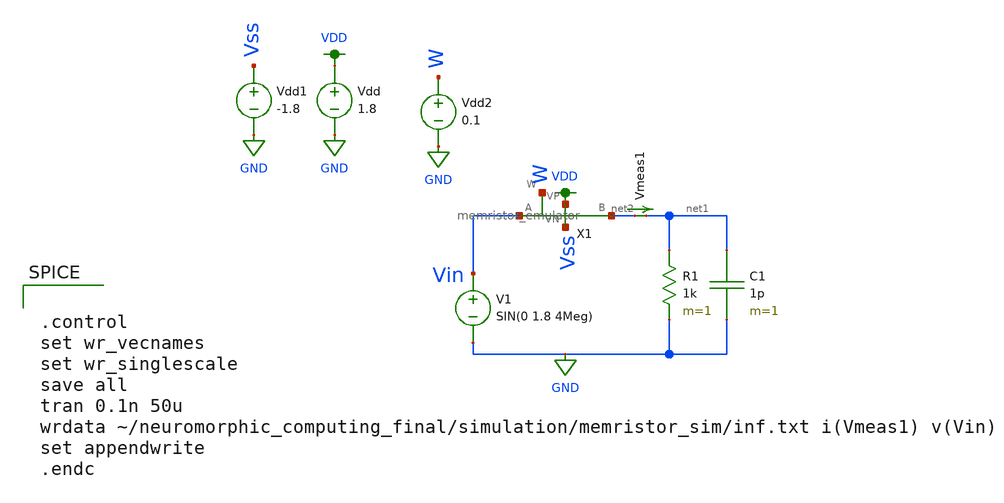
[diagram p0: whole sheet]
** sch_path: schematic/infinite.sch
**.subckt infinite
V1 Vin GND SIN(0 1.8 4Meg)
R1 net1 GND 1k m=1
C1 net1 GND 1p m=1
Vdd VDD GND 1.8
Vmeas1 net2 net1 0
.save i(vmeas1)
Vdd1 Vss GND -1.8
X1 VDD Vss net2 Vin W memristor_emulator
Vdd2 W GND 0.1
**** begin user architecture code


.control
set wr_vecnames
set wr_singlescale
save all
tran 0.1n 50u
wrdata ~/neuromorphic_computing_final/simulation/memristor_sim/inf.txt i(Vmeas1) v(Vin)
set appendwrite
.endc



.option wnflag=1
.param MC_SWITCH=0.0
.lib ~/skywater/skywater-pdk/libraries/sky130_fd_pr_ngspice/latest/models/sky130.lib.spice tt

**** end user architecture code
**.ends

* expanding   symbol:  /home/madvlsi/neuromorphic_computing_final/schematic/memristor_emulator.sym #
*+ of pins=5
** sym_path: schematic/memristor_emulator.sym
** sch_path: schematic/memristor_emulator.sch
.subckt memristor_emulator VP VN B A W
*.ipin A
*.iopin VN
*.iopin VP
*.opin B
*.opin W
XM1 B W A B sky130_fd_pr__pfet_01v8 L=0.5 W=12 nf=1 ad='int((nf+1)/2) * W/nf * 0.29' as='int((nf+2)/2) * W/nf * 0.29'
+ pd='2*int((nf+1)/2) * (W/nf + 0.29)' ps='2*int((nf+2)/2) * (W/nf + 0.29)' nrd='0.29 / W' nrs='0.29 / W'
+ sa=0 sb=0 sd=0 mult=1 m=1
XM2 VP A W VP sky130_fd_pr__pfet_01v8 L=2 W=3 nf=1 ad='int((nf+1)/2) * W/nf * 0.29' as='int((nf+2)/2) * W/nf * 0.29'
+ pd='2*int((nf+1)/2) * (W/nf + 0.29)' ps='2*int((nf+2)/2) * (W/nf + 0.29)' nrd='0.29 / W' nrs='0.29 / W'
+ sa=0 sb=0 sd=0 mult=1 m=1
XM3 VN W VN VN sky130_fd_pr__nfet_01v8 L=20 W=20 nf=1 ad='int((nf+1)/2) * W/nf * 0.29' as='int((nf+2)/2) * W/nf * 0.29'
+ pd='2*int((nf+1)/2) * (W/nf + 0.29)' ps='2*int((nf+2)/2) * (W/nf + 0.29)' nrd='0.29 / W' nrs='0.29 / W'
+ sa=0 sb=0 sd=0 mult=1 m=1
XM4 VN B W VN sky130_fd_pr__nfet_01v8 L=3 W=2 nf=1 ad='int((nf+1)/2) * W/nf * 0.29' as='int((nf+2)/2) * W/nf * 0.29'
+ pd='2*int((nf+1)/2) * (W/nf + 0.29)' ps='2*int((nf+2)/2) * (W/nf + 0.29)' nrd='0.29 / W' nrs='0.29 / W'
+ sa=0 sb=0 sd=0 mult=1 m=1
.ends

.GLOBAL VDD
.GLOBAL GND
.end
